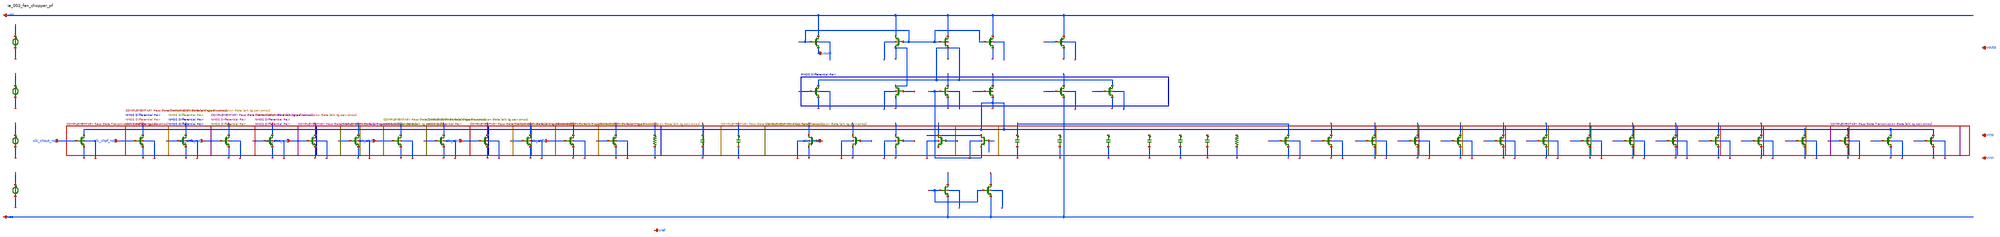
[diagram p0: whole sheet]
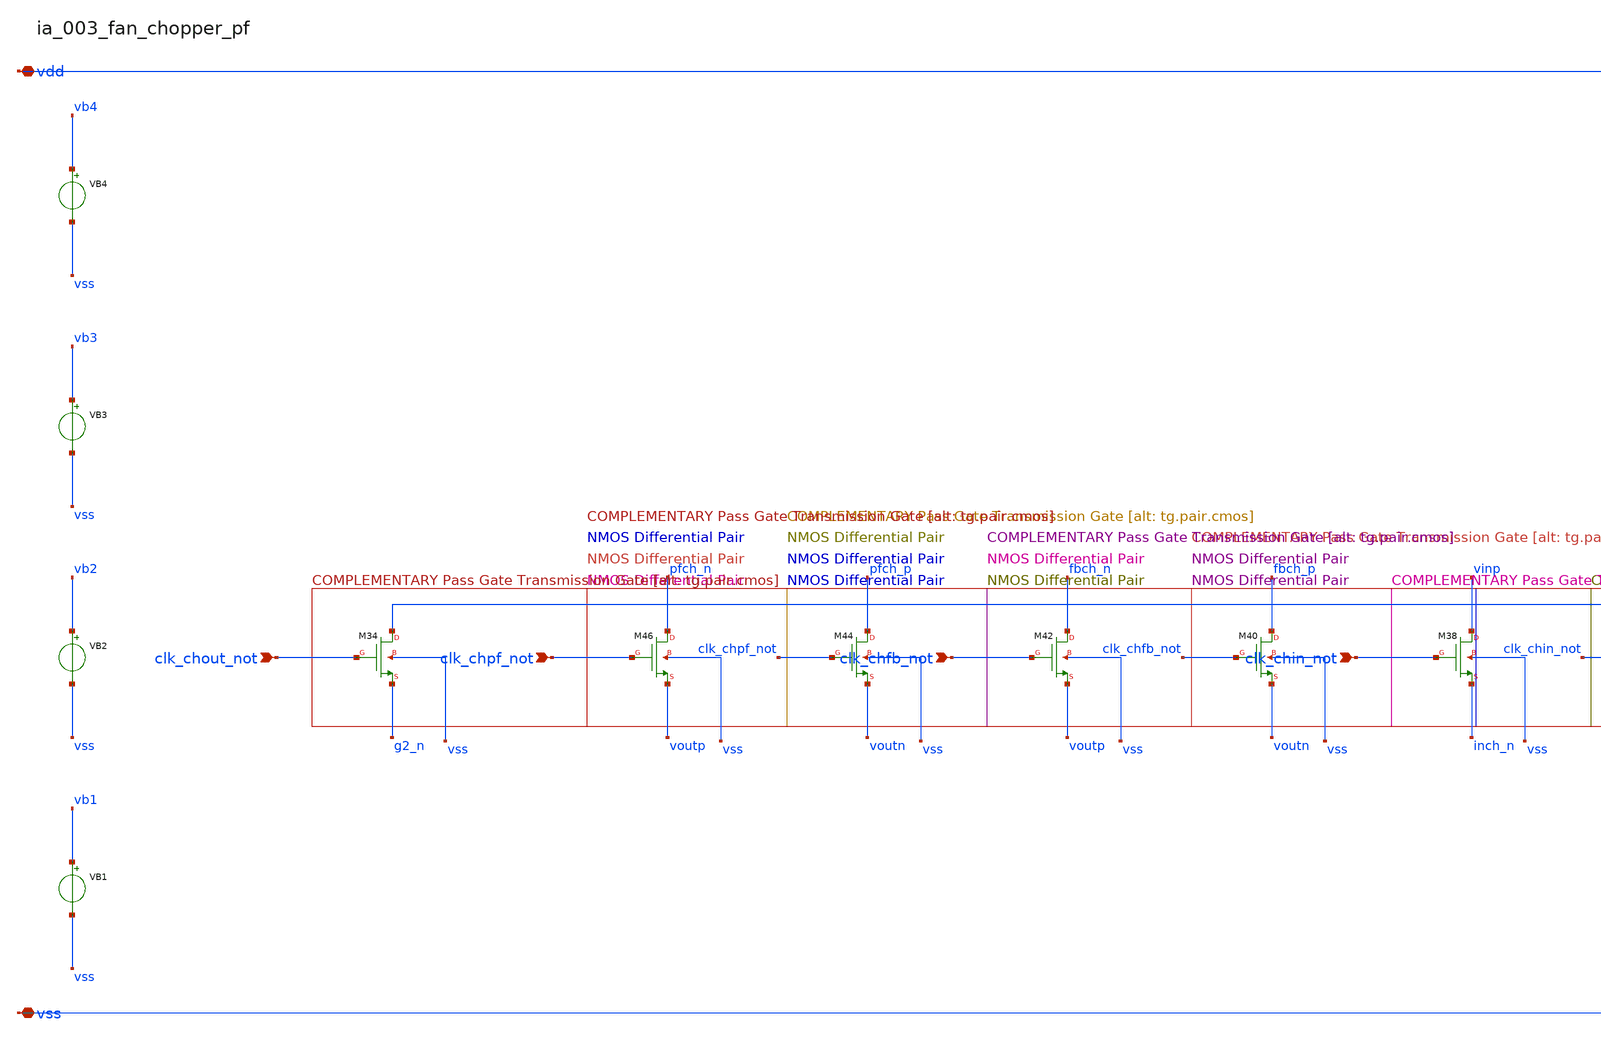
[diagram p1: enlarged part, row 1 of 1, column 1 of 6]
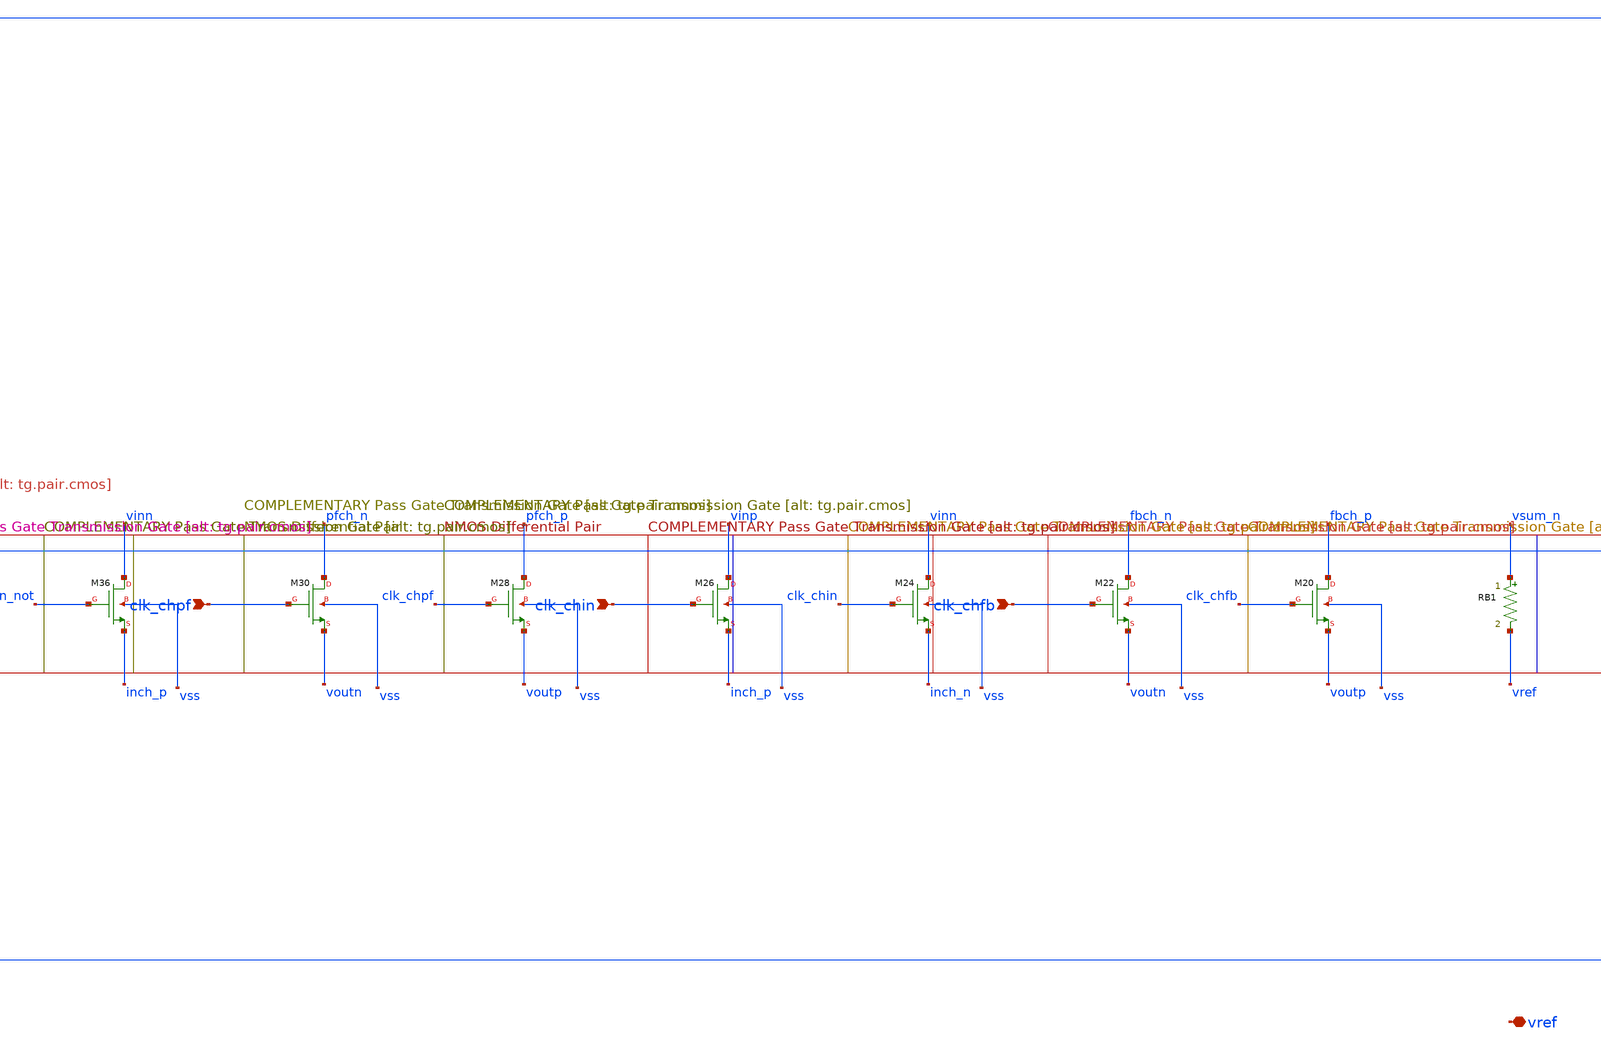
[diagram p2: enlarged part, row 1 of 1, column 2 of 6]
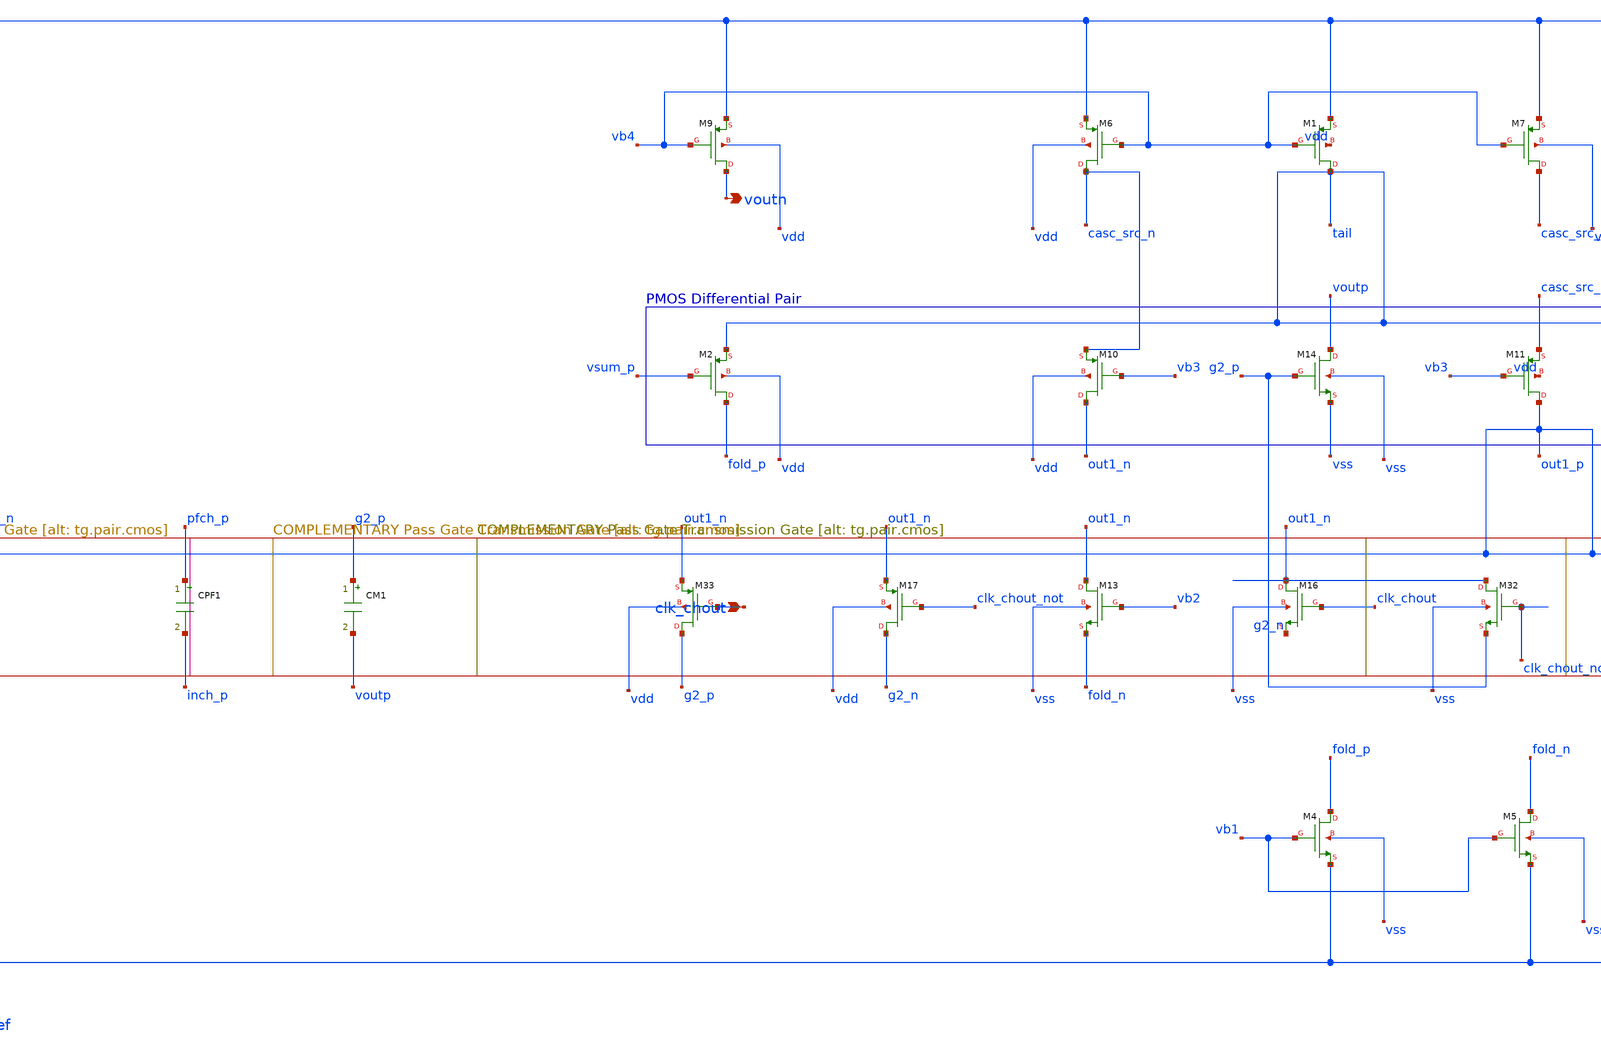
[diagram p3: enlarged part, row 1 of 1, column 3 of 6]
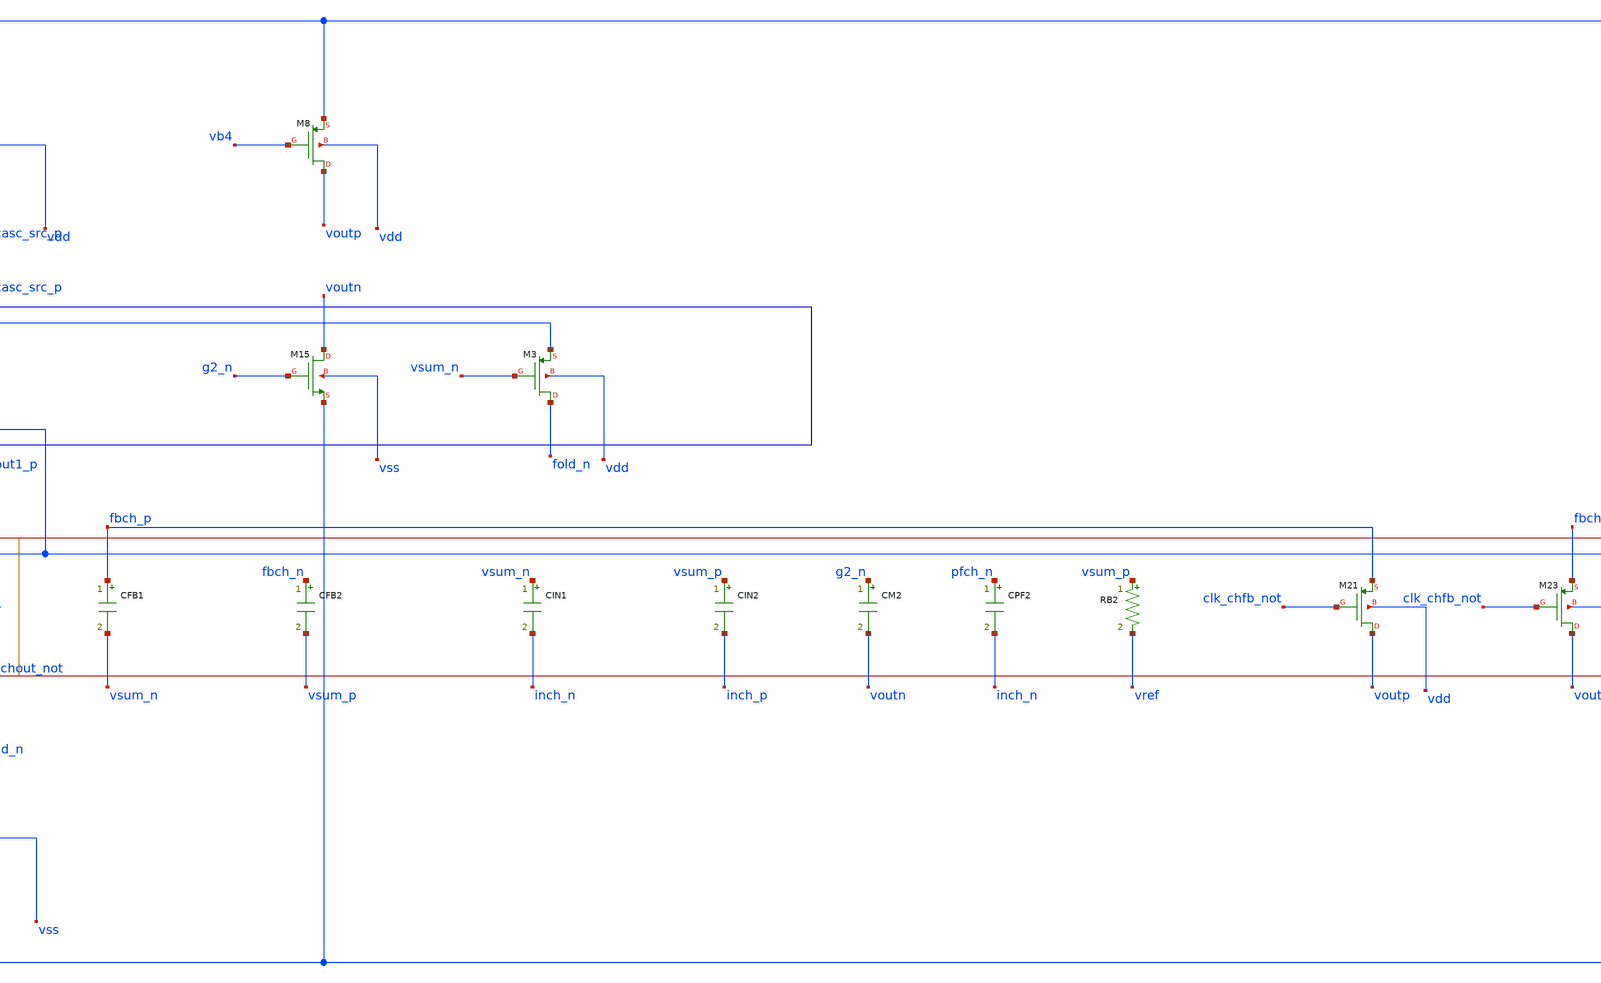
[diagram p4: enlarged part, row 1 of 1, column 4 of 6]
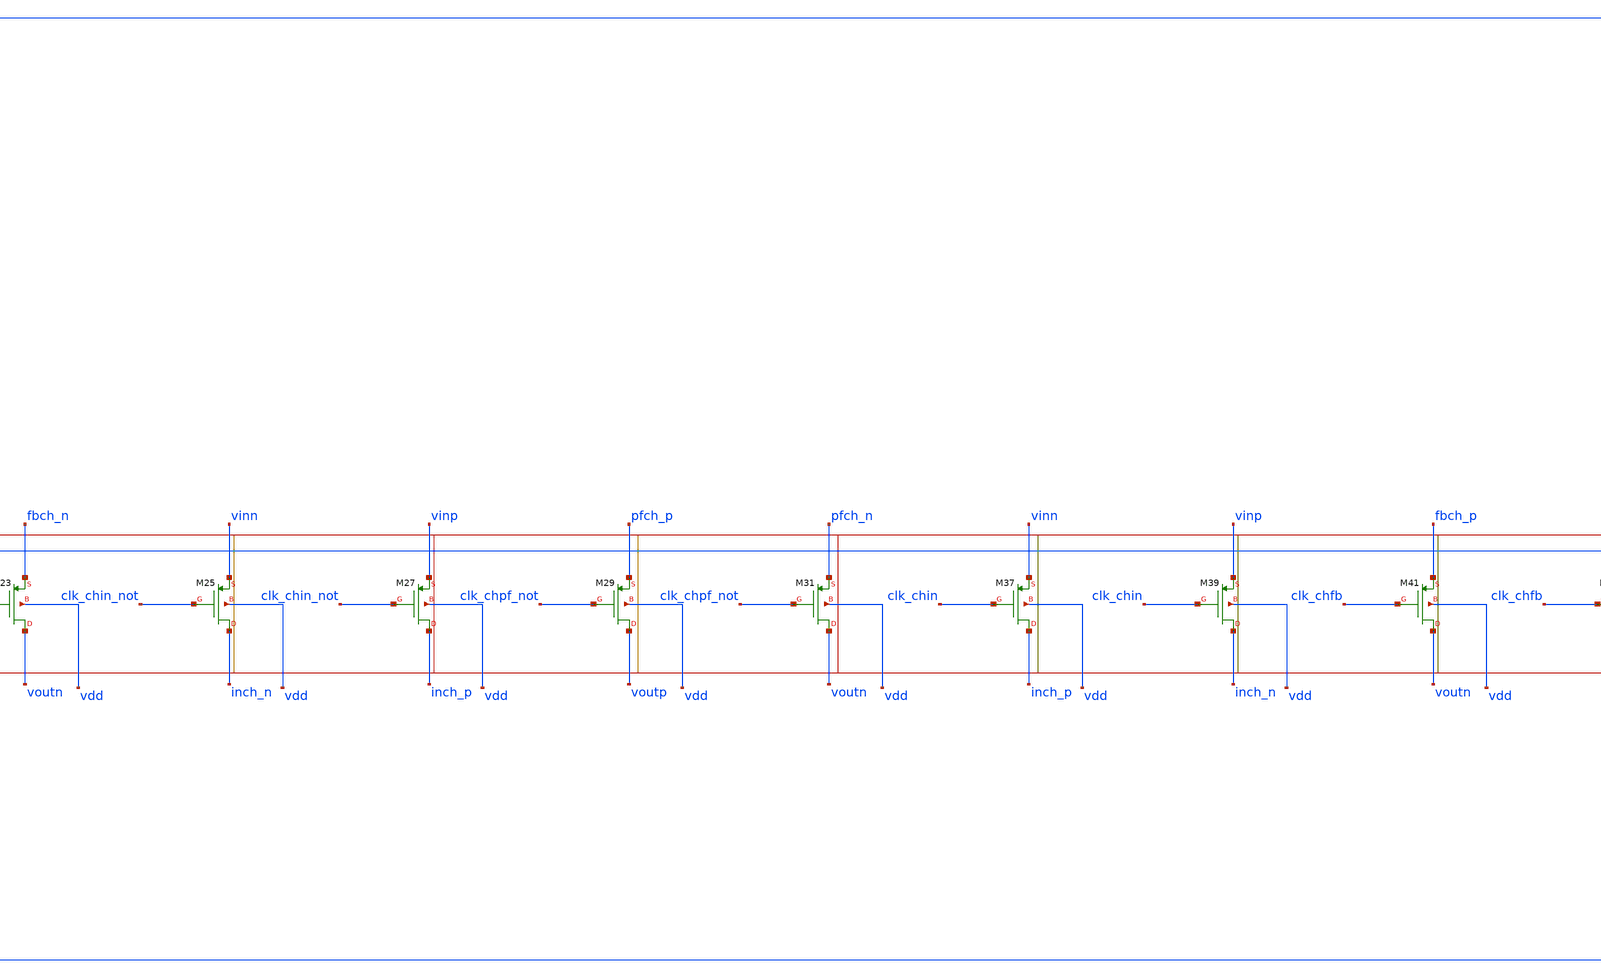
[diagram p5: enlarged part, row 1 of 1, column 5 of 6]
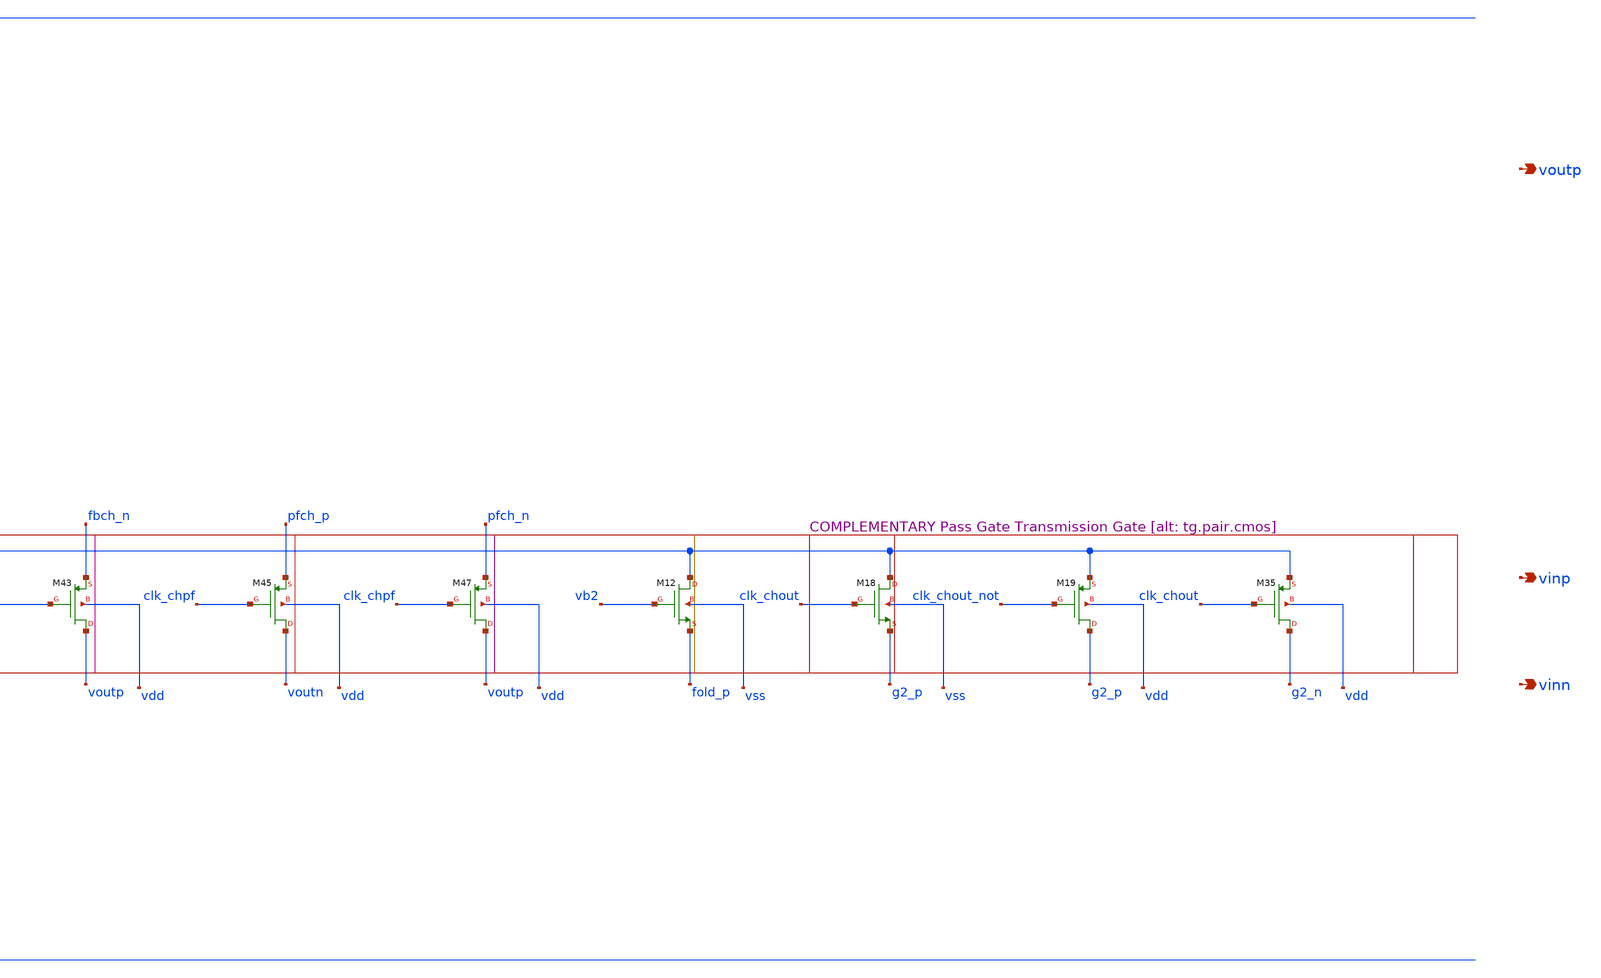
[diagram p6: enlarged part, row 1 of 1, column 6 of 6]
** sch_path: analog-db/raw/ia_003_fan_chopper_pf/ia_003_fan_chopper_pf_annotated.sch
**.subckt ia_003_fan_chopper_pf_annotated clk_chout_not clk_chpf_not clk_chfb_not clk_chin_not
*+ clk_chpf clk_chin clk_chfb clk_chout vdd vss voutn vref voutp vinp vinn
*.ipin clk_chout_not
*.ipin clk_chpf_not
*.ipin clk_chfb_not
*.ipin clk_chin_not
*.ipin clk_chpf
*.ipin clk_chin
*.ipin clk_chfb
*.ipin clk_chout
*.iopin vdd
*.iopin vss
*.opin voutn
*.iopin vref
*.opin voutp
*.opin vinp
*.opin vinn
CFB1 fbch_p vsum_n 'x_dut_cfb1_value' m=1
CFB2 fbch_n vsum_p 'x_dut_cfb2_value' m=1
CIN1 vsum_n inch_n 'x_dut_cin1_value' m=1
CIN2 vsum_p inch_p 'x_dut_cin2_value' m=1
CM1 g2_p voutp 'x_dut_cm1_value' m=1
CM2 g2_n voutn 'x_dut_cm2_value' m=1
CPF1 pfch_p inch_p 'x_dut_cpf1_value' m=1
CPF2 pfch_n inch_n 'x_dut_cpf2_value' m=1
RB1 vsum_n vref 'x_dut_rb1_value' m=1
RB2 vsum_p vref 'x_dut_rb2_value' m=1
VB1 vb1 vss dc {vb1}
VB2 vb2 vss dc {vb2}
VB3 vb3 vss dc {vb3}
VB4 vb4 vss dc {vb4}
XM1 tail vb4 vdd vdd sg13_lv_pmos w=x_dut_xm1_w l=x_dut_xm1_l ng=1 m=x_dut_xm1_m
XM10 out1_n vb3 casc_src_n vdd sg13_lv_pmos w=x_dut_xm10_w l=x_dut_xm10_l ng=1 m=x_dut_xm10_m
XM11 out1_p vb3 casc_src_p vdd sg13_lv_pmos w=x_dut_xm11_w l=x_dut_xm11_l ng=1 m=x_dut_xm11_m
XM12 out1_p vb2 fold_p vss sg13_lv_nmos w=x_dut_xm12_w l=x_dut_xm12_l ng=1 m=x_dut_xm12_m
XM13 out1_n vb2 fold_n vss sg13_lv_nmos w=x_dut_xm13_w l=x_dut_xm13_l ng=1 m=x_dut_xm13_m
XM14 voutp g2_p vss vss sg13_lv_nmos w=x_dut_xm14_w l=x_dut_xm14_l ng=1 m=x_dut_xm14_m
XM15 voutn g2_n vss vss sg13_lv_nmos w=x_dut_xm15_w l=x_dut_xm15_l ng=1 m=x_dut_xm15_m
XM16 out1_n clk_chout g2_n vss sg13_lv_nmos w=x_dut_xm16_w l=x_dut_xm16_l ng=1 m=x_dut_xm16_m
XM17 g2_n clk_chout_not out1_n vdd sg13_lv_pmos w=x_dut_xm17_w l=x_dut_xm17_l ng=1 m=x_dut_xm17_m
XM18 out1_p clk_chout g2_p vss sg13_lv_nmos w=x_dut_xm18_w l=x_dut_xm18_l ng=1 m=x_dut_xm18_m
XM19 g2_p clk_chout_not out1_p vdd sg13_lv_pmos w=x_dut_xm19_w l=x_dut_xm19_l ng=1 m=x_dut_xm19_m
XM2 fold_p vsum_p tail vdd sg13_lv_pmos w=x_dut_xm2_w l=x_dut_xm2_l ng=1 m=x_dut_xm2_m
XM20 fbch_p clk_chfb voutp vss sg13_lv_nmos w=x_dut_xm20_w l=x_dut_xm20_l ng=1 m=x_dut_xm20_m
XM21 voutp clk_chfb_not fbch_p vdd sg13_lv_pmos w=x_dut_xm21_w l=x_dut_xm21_l ng=1 m=x_dut_xm21_m
XM22 fbch_n clk_chfb voutn vss sg13_lv_nmos w=x_dut_xm22_w l=x_dut_xm22_l ng=1 m=x_dut_xm22_m
XM23 voutn clk_chfb_not fbch_n vdd sg13_lv_pmos w=x_dut_xm23_w l=x_dut_xm23_l ng=1 m=x_dut_xm23_m
XM24 vinn clk_chin inch_n vss sg13_lv_nmos w=x_dut_xm24_w l=x_dut_xm24_l ng=1 m=x_dut_xm24_m
XM25 inch_n clk_chin_not vinn vdd sg13_lv_pmos w=x_dut_xm25_w l=x_dut_xm25_l ng=1 m=x_dut_xm25_m
XM26 vinp clk_chin inch_p vss sg13_lv_nmos w=x_dut_xm26_w l=x_dut_xm26_l ng=1 m=x_dut_xm26_m
XM27 inch_p clk_chin_not vinp vdd sg13_lv_pmos w=x_dut_xm27_w l=x_dut_xm27_l ng=1 m=x_dut_xm27_m
XM28 pfch_p clk_chpf voutp vss sg13_lv_nmos w=x_dut_xm28_w l=x_dut_xm28_l ng=1 m=x_dut_xm28_m
XM29 voutp clk_chpf_not pfch_p vdd sg13_lv_pmos w=x_dut_xm29_w l=x_dut_xm29_l ng=1 m=x_dut_xm29_m
XM3 fold_n vsum_n tail vdd sg13_lv_pmos w=x_dut_xm3_w l=x_dut_xm3_l ng=1 m=x_dut_xm3_m
XM30 pfch_n clk_chpf voutn vss sg13_lv_nmos w=x_dut_xm30_w l=x_dut_xm30_l ng=1 m=x_dut_xm30_m
XM31 voutn clk_chpf_not pfch_n vdd sg13_lv_pmos w=x_dut_xm31_w l=x_dut_xm31_l ng=1 m=x_dut_xm31_m
XM32 out1_n clk_chout_not g2_p vss sg13_lv_nmos w=x_dut_xm32_w l=x_dut_xm32_l ng=1 m=x_dut_xm32_m
XM33 g2_p clk_chout out1_n vdd sg13_lv_pmos w=x_dut_xm33_w l=x_dut_xm33_l ng=1 m=x_dut_xm33_m
XM34 out1_p clk_chout_not g2_n vss sg13_lv_nmos w=x_dut_xm34_w l=x_dut_xm34_l ng=1 m=x_dut_xm34_m
XM35 g2_n clk_chout out1_p vdd sg13_lv_pmos w=x_dut_xm35_w l=x_dut_xm35_l ng=1 m=x_dut_xm35_m
XM36 vinn clk_chin_not inch_p vss sg13_lv_nmos w=x_dut_xm36_w l=x_dut_xm36_l ng=1 m=x_dut_xm36_m
XM37 inch_p clk_chin vinn vdd sg13_lv_pmos w=x_dut_xm37_w l=x_dut_xm37_l ng=1 m=x_dut_xm37_m
XM38 vinp clk_chin_not inch_n vss sg13_lv_nmos w=x_dut_xm38_w l=x_dut_xm38_l ng=1 m=x_dut_xm38_m
XM39 inch_n clk_chin vinp vdd sg13_lv_pmos w=x_dut_xm39_w l=x_dut_xm39_l ng=1 m=x_dut_xm39_m
XM4 fold_p vb1 vss vss sg13_lv_nmos w=x_dut_xm4_w l=x_dut_xm4_l ng=1 m=x_dut_xm4_m
XM40 fbch_p clk_chfb_not voutn vss sg13_lv_nmos w=x_dut_xm40_w l=x_dut_xm40_l ng=1 m=x_dut_xm40_m
XM41 voutn clk_chfb fbch_p vdd sg13_lv_pmos w=x_dut_xm41_w l=x_dut_xm41_l ng=1 m=x_dut_xm41_m
XM42 fbch_n clk_chfb_not voutp vss sg13_lv_nmos w=x_dut_xm42_w l=x_dut_xm42_l ng=1 m=x_dut_xm42_m
XM43 voutp clk_chfb fbch_n vdd sg13_lv_pmos w=x_dut_xm43_w l=x_dut_xm43_l ng=1 m=x_dut_xm43_m
XM44 pfch_p clk_chpf_not voutn vss sg13_lv_nmos w=x_dut_xm44_w l=x_dut_xm44_l ng=1 m=x_dut_xm44_m
XM45 voutn clk_chpf pfch_p vdd sg13_lv_pmos w=x_dut_xm45_w l=x_dut_xm45_l ng=1 m=x_dut_xm45_m
XM46 pfch_n clk_chpf_not voutp vss sg13_lv_nmos w=x_dut_xm46_w l=x_dut_xm46_l ng=1 m=x_dut_xm46_m
XM47 voutp clk_chpf pfch_n vdd sg13_lv_pmos w=x_dut_xm47_w l=x_dut_xm47_l ng=1 m=x_dut_xm47_m
XM5 fold_n vb1 vss vss sg13_lv_nmos w=x_dut_xm5_w l=x_dut_xm5_l ng=1 m=x_dut_xm5_m
XM6 casc_src_n vb4 vdd vdd sg13_lv_pmos w=x_dut_xm6_w l=x_dut_xm6_l ng=1 m=x_dut_xm6_m
XM7 casc_src_p vb4 vdd vdd sg13_lv_pmos w=x_dut_xm7_w l=x_dut_xm7_l ng=1 m=x_dut_xm7_m
XM8 voutp vb4 vdd vdd sg13_lv_pmos w=x_dut_xm8_w l=x_dut_xm8_l ng=1 m=x_dut_xm8_m
XM9 voutn vb4 vdd vdd sg13_lv_pmos w=x_dut_xm9_w l=x_dut_xm9_l ng=1 m=x_dut_xm9_m
**.ends
.end
